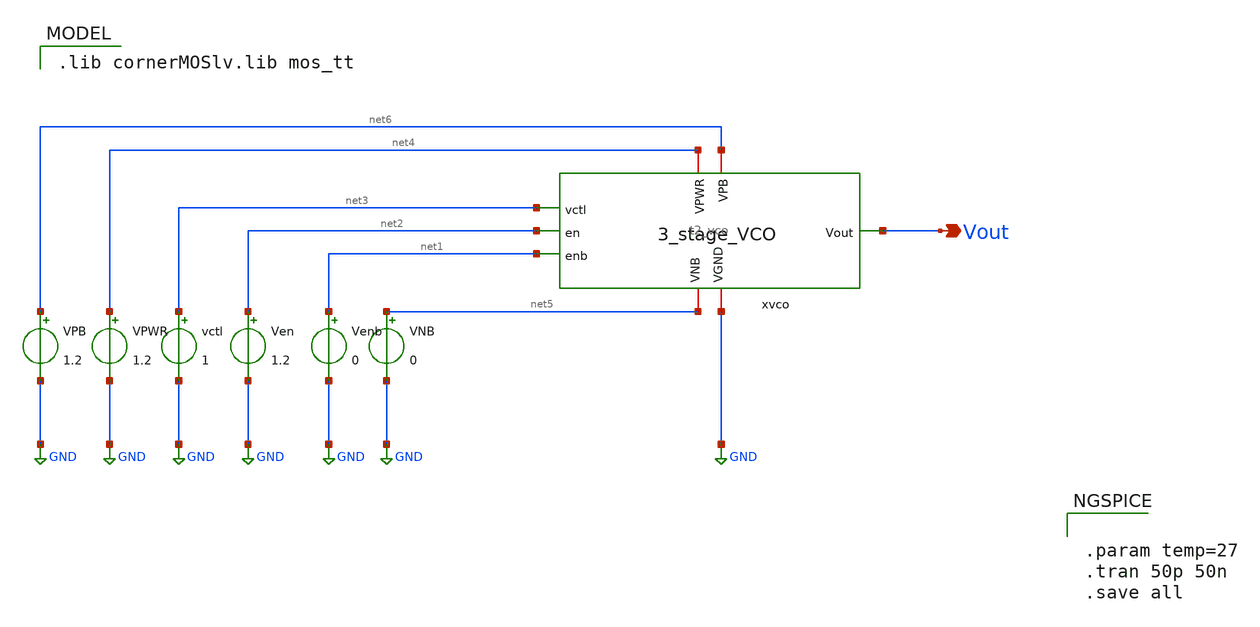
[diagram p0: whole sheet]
** sch_path: Team Designs/Team 2 Design/design_data/xschem/t2_vco_tb.sch
**.subckt t2_vco_tb Vout
*.opin Vout
VPWR net4 GND 1.2
vctl net3 GND 1
Ven net2 GND 1.2
Venb net1 GND 0
VNB net5 GND 0
VPB net6 GND 1.2
x1 net4 net6 GND net5 Vout net3 net2 net1 t2_vco
**** begin user architecture code
 .lib cornerMOSlv.lib mos_tt



.param temp=27
.tran 50p 50n
.save all


**** end user architecture code
**.ends
.GLOBAL GND
.end
